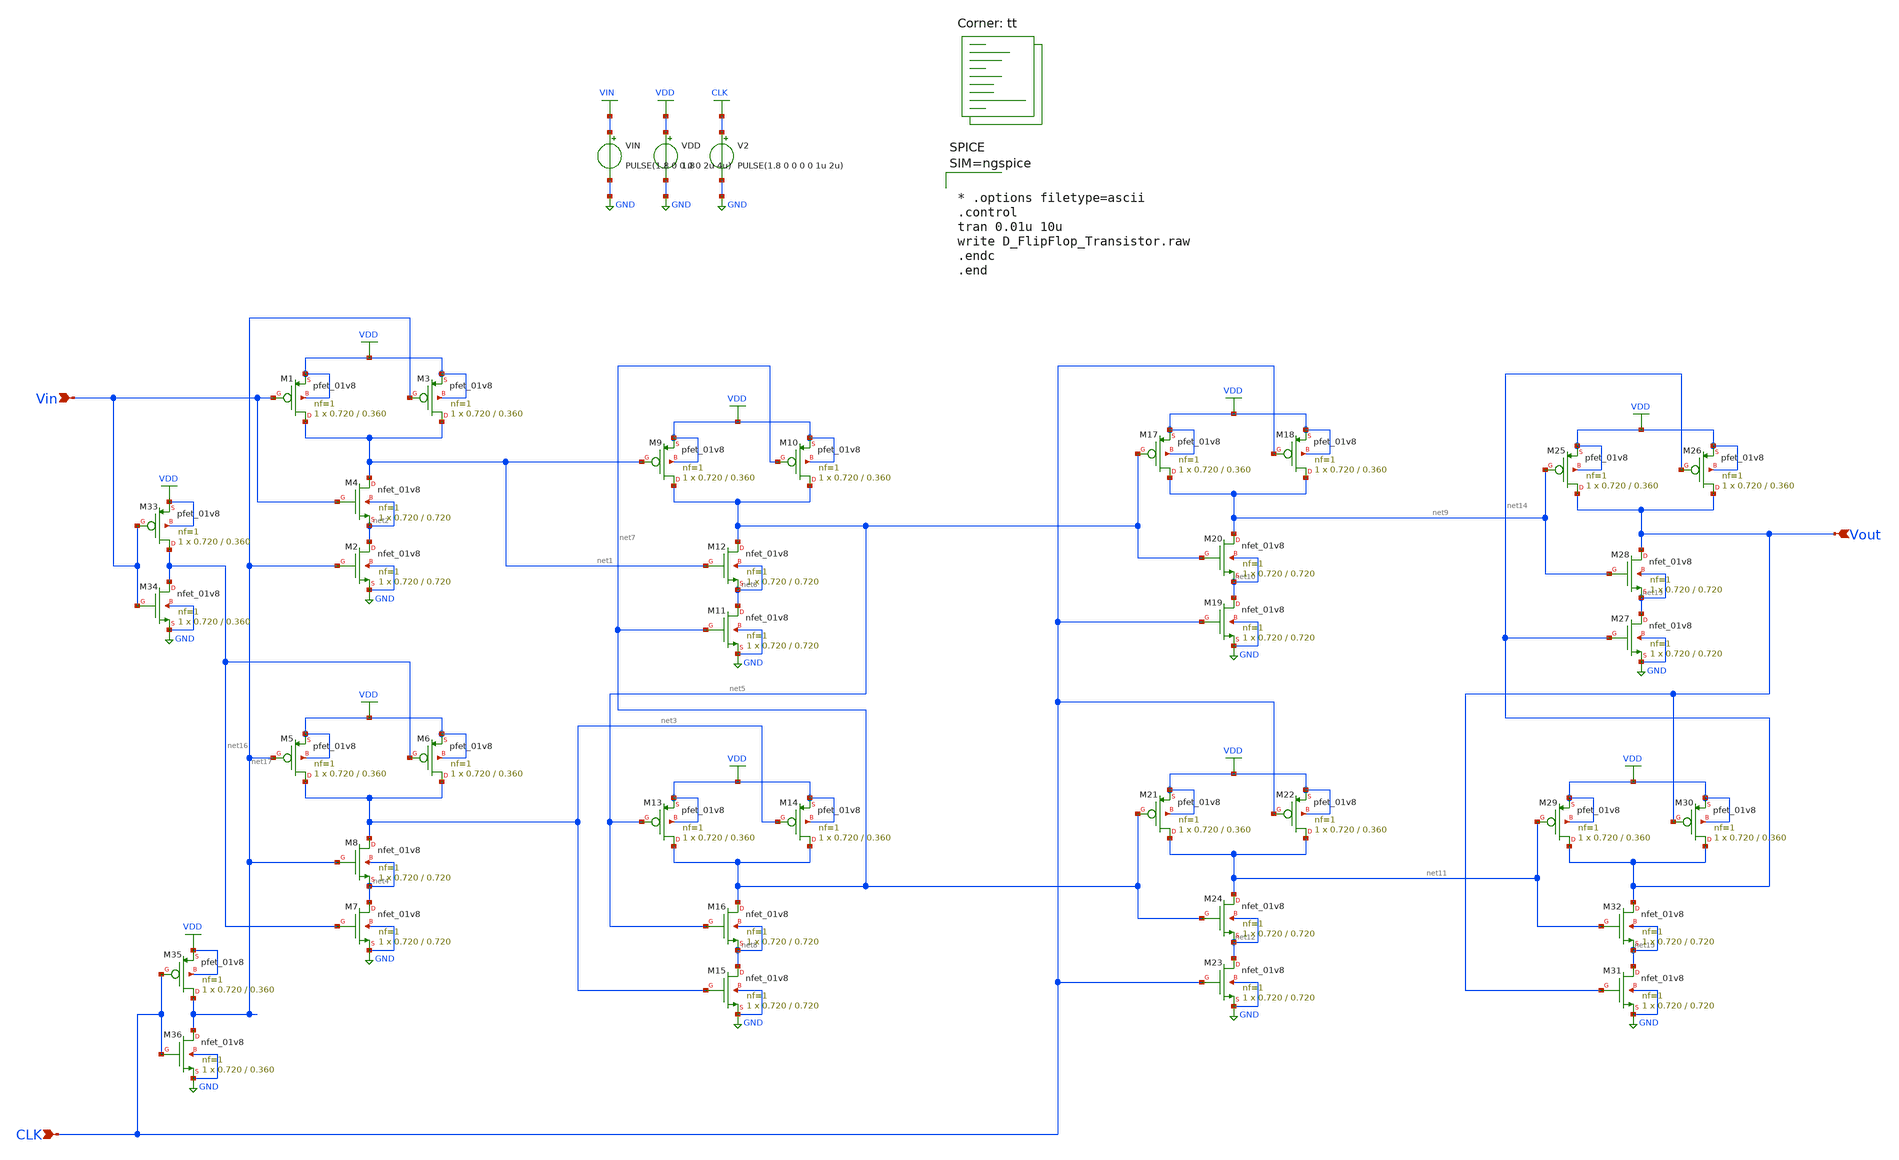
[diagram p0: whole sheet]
** sch_path: xschem/D_FlipFlop_Transistor.sch
**.subckt D_FlipFlop_Transistor CLK Vin Vout
*.ipin CLK
*.ipin Vin
*.ipin Vout
XM1 net1 Vin VDD VDD sky130_fd_pr__pfet_01v8 L=0.360 W=0.720 nf=1 ad='int((nf+1)/2) * W/nf * 0.29' as='int((nf+2)/2) * W/nf * 0.29'
+ pd='2*int((nf+1)/2) * (W/nf + 0.29)' ps='2*int((nf+2)/2) * (W/nf + 0.29)' nrd='0.29 / W' nrs='0.29 / W'
+ sa=0 sb=0 sd=0 mult=1 m=1
XM3 net1 net17 VDD VDD sky130_fd_pr__pfet_01v8 L=0.360 W=0.720 nf=1 ad='int((nf+1)/2) * W/nf * 0.29'
+ as='int((nf+2)/2) * W/nf * 0.29' pd='2*int((nf+1)/2) * (W/nf + 0.29)' ps='2*int((nf+2)/2) * (W/nf + 0.29)'
+ nrd='0.29 / W' nrs='0.29 / W' sa=0 sb=0 sd=0 mult=1 m=1
XM2 net2 net17 GND GND sky130_fd_pr__nfet_01v8 L=0.720 W=0.720 nf=1 ad='int((nf+1)/2) * W/nf * 0.29'
+ as='int((nf+2)/2) * W/nf * 0.29' pd='2*int((nf+1)/2) * (W/nf + 0.29)' ps='2*int((nf+2)/2) * (W/nf + 0.29)'
+ nrd='0.29 / W' nrs='0.29 / W' sa=0 sb=0 sd=0 mult=1 m=1
XM4 net1 Vin net2 net2 sky130_fd_pr__nfet_01v8 L=0.720 W=0.720 nf=1 ad='int((nf+1)/2) * W/nf * 0.29'
+ as='int((nf+2)/2) * W/nf * 0.29' pd='2*int((nf+1)/2) * (W/nf + 0.29)' ps='2*int((nf+2)/2) * (W/nf + 0.29)'
+ nrd='0.29 / W' nrs='0.29 / W' sa=0 sb=0 sd=0 mult=1 m=1
XM5 net3 net17 VDD VDD sky130_fd_pr__pfet_01v8 L=0.360 W=0.720 nf=1 ad='int((nf+1)/2) * W/nf * 0.29'
+ as='int((nf+2)/2) * W/nf * 0.29' pd='2*int((nf+1)/2) * (W/nf + 0.29)' ps='2*int((nf+2)/2) * (W/nf + 0.29)'
+ nrd='0.29 / W' nrs='0.29 / W' sa=0 sb=0 sd=0 mult=1 m=1
XM6 net3 net16 VDD VDD sky130_fd_pr__pfet_01v8 L=0.360 W=0.720 nf=1 ad='int((nf+1)/2) * W/nf * 0.29'
+ as='int((nf+2)/2) * W/nf * 0.29' pd='2*int((nf+1)/2) * (W/nf + 0.29)' ps='2*int((nf+2)/2) * (W/nf + 0.29)'
+ nrd='0.29 / W' nrs='0.29 / W' sa=0 sb=0 sd=0 mult=1 m=1
XM7 net4 net16 GND GND sky130_fd_pr__nfet_01v8 L=0.720 W=0.720 nf=1 ad='int((nf+1)/2) * W/nf * 0.29'
+ as='int((nf+2)/2) * W/nf * 0.29' pd='2*int((nf+1)/2) * (W/nf + 0.29)' ps='2*int((nf+2)/2) * (W/nf + 0.29)'
+ nrd='0.29 / W' nrs='0.29 / W' sa=0 sb=0 sd=0 mult=1 m=1
XM8 net3 net17 net4 net4 sky130_fd_pr__nfet_01v8 L=0.720 W=0.720 nf=1 ad='int((nf+1)/2) * W/nf * 0.29'
+ as='int((nf+2)/2) * W/nf * 0.29' pd='2*int((nf+1)/2) * (W/nf + 0.29)' ps='2*int((nf+2)/2) * (W/nf + 0.29)'
+ nrd='0.29 / W' nrs='0.29 / W' sa=0 sb=0 sd=0 mult=1 m=1
XM9 net5 net1 VDD VDD sky130_fd_pr__pfet_01v8 L=0.360 W=0.720 nf=1 ad='int((nf+1)/2) * W/nf * 0.29' as='int((nf+2)/2) * W/nf * 0.29'
+ pd='2*int((nf+1)/2) * (W/nf + 0.29)' ps='2*int((nf+2)/2) * (W/nf + 0.29)' nrd='0.29 / W' nrs='0.29 / W'
+ sa=0 sb=0 sd=0 mult=1 m=1
XM10 net5 net7 VDD VDD sky130_fd_pr__pfet_01v8 L=0.360 W=0.720 nf=1 ad='int((nf+1)/2) * W/nf * 0.29'
+ as='int((nf+2)/2) * W/nf * 0.29' pd='2*int((nf+1)/2) * (W/nf + 0.29)' ps='2*int((nf+2)/2) * (W/nf + 0.29)'
+ nrd='0.29 / W' nrs='0.29 / W' sa=0 sb=0 sd=0 mult=1 m=1
XM11 net6 net7 GND GND sky130_fd_pr__nfet_01v8 L=0.720 W=0.720 nf=1 ad='int((nf+1)/2) * W/nf * 0.29'
+ as='int((nf+2)/2) * W/nf * 0.29' pd='2*int((nf+1)/2) * (W/nf + 0.29)' ps='2*int((nf+2)/2) * (W/nf + 0.29)'
+ nrd='0.29 / W' nrs='0.29 / W' sa=0 sb=0 sd=0 mult=1 m=1
XM12 net5 net1 net6 net6 sky130_fd_pr__nfet_01v8 L=0.720 W=0.720 nf=1 ad='int((nf+1)/2) * W/nf * 0.29'
+ as='int((nf+2)/2) * W/nf * 0.29' pd='2*int((nf+1)/2) * (W/nf + 0.29)' ps='2*int((nf+2)/2) * (W/nf + 0.29)'
+ nrd='0.29 / W' nrs='0.29 / W' sa=0 sb=0 sd=0 mult=1 m=1
XM13 net7 net5 VDD VDD sky130_fd_pr__pfet_01v8 L=0.360 W=0.720 nf=1 ad='int((nf+1)/2) * W/nf * 0.29'
+ as='int((nf+2)/2) * W/nf * 0.29' pd='2*int((nf+1)/2) * (W/nf + 0.29)' ps='2*int((nf+2)/2) * (W/nf + 0.29)'
+ nrd='0.29 / W' nrs='0.29 / W' sa=0 sb=0 sd=0 mult=1 m=1
XM14 net7 net3 VDD VDD sky130_fd_pr__pfet_01v8 L=0.360 W=0.720 nf=1 ad='int((nf+1)/2) * W/nf * 0.29'
+ as='int((nf+2)/2) * W/nf * 0.29' pd='2*int((nf+1)/2) * (W/nf + 0.29)' ps='2*int((nf+2)/2) * (W/nf + 0.29)'
+ nrd='0.29 / W' nrs='0.29 / W' sa=0 sb=0 sd=0 mult=1 m=1
XM15 net8 net3 GND GND sky130_fd_pr__nfet_01v8 L=0.720 W=0.720 nf=1 ad='int((nf+1)/2) * W/nf * 0.29'
+ as='int((nf+2)/2) * W/nf * 0.29' pd='2*int((nf+1)/2) * (W/nf + 0.29)' ps='2*int((nf+2)/2) * (W/nf + 0.29)'
+ nrd='0.29 / W' nrs='0.29 / W' sa=0 sb=0 sd=0 mult=1 m=1
XM16 net7 net5 net8 net8 sky130_fd_pr__nfet_01v8 L=0.720 W=0.720 nf=1 ad='int((nf+1)/2) * W/nf * 0.29'
+ as='int((nf+2)/2) * W/nf * 0.29' pd='2*int((nf+1)/2) * (W/nf + 0.29)' ps='2*int((nf+2)/2) * (W/nf + 0.29)'
+ nrd='0.29 / W' nrs='0.29 / W' sa=0 sb=0 sd=0 mult=1 m=1
XM17 net9 net5 VDD VDD sky130_fd_pr__pfet_01v8 L=0.360 W=0.720 nf=1 ad='int((nf+1)/2) * W/nf * 0.29'
+ as='int((nf+2)/2) * W/nf * 0.29' pd='2*int((nf+1)/2) * (W/nf + 0.29)' ps='2*int((nf+2)/2) * (W/nf + 0.29)'
+ nrd='0.29 / W' nrs='0.29 / W' sa=0 sb=0 sd=0 mult=1 m=1
XM18 net9 CLK VDD VDD sky130_fd_pr__pfet_01v8 L=0.360 W=0.720 nf=1 ad='int((nf+1)/2) * W/nf * 0.29' as='int((nf+2)/2) * W/nf * 0.29'
+ pd='2*int((nf+1)/2) * (W/nf + 0.29)' ps='2*int((nf+2)/2) * (W/nf + 0.29)' nrd='0.29 / W' nrs='0.29 / W'
+ sa=0 sb=0 sd=0 mult=1 m=1
XM19 net10 CLK GND GND sky130_fd_pr__nfet_01v8 L=0.720 W=0.720 nf=1 ad='int((nf+1)/2) * W/nf * 0.29'
+ as='int((nf+2)/2) * W/nf * 0.29' pd='2*int((nf+1)/2) * (W/nf + 0.29)' ps='2*int((nf+2)/2) * (W/nf + 0.29)'
+ nrd='0.29 / W' nrs='0.29 / W' sa=0 sb=0 sd=0 mult=1 m=1
XM20 net9 net5 net10 net10 sky130_fd_pr__nfet_01v8 L=0.720 W=0.720 nf=1 ad='int((nf+1)/2) * W/nf * 0.29'
+ as='int((nf+2)/2) * W/nf * 0.29' pd='2*int((nf+1)/2) * (W/nf + 0.29)' ps='2*int((nf+2)/2) * (W/nf + 0.29)'
+ nrd='0.29 / W' nrs='0.29 / W' sa=0 sb=0 sd=0 mult=1 m=1
XM21 net11 net7 VDD VDD sky130_fd_pr__pfet_01v8 L=0.360 W=0.720 nf=1 ad='int((nf+1)/2) * W/nf * 0.29'
+ as='int((nf+2)/2) * W/nf * 0.29' pd='2*int((nf+1)/2) * (W/nf + 0.29)' ps='2*int((nf+2)/2) * (W/nf + 0.29)'
+ nrd='0.29 / W' nrs='0.29 / W' sa=0 sb=0 sd=0 mult=1 m=1
XM22 net11 CLK VDD VDD sky130_fd_pr__pfet_01v8 L=0.360 W=0.720 nf=1 ad='int((nf+1)/2) * W/nf * 0.29'
+ as='int((nf+2)/2) * W/nf * 0.29' pd='2*int((nf+1)/2) * (W/nf + 0.29)' ps='2*int((nf+2)/2) * (W/nf + 0.29)'
+ nrd='0.29 / W' nrs='0.29 / W' sa=0 sb=0 sd=0 mult=1 m=1
XM23 net12 CLK GND GND sky130_fd_pr__nfet_01v8 L=0.720 W=0.720 nf=1 ad='int((nf+1)/2) * W/nf * 0.29'
+ as='int((nf+2)/2) * W/nf * 0.29' pd='2*int((nf+1)/2) * (W/nf + 0.29)' ps='2*int((nf+2)/2) * (W/nf + 0.29)'
+ nrd='0.29 / W' nrs='0.29 / W' sa=0 sb=0 sd=0 mult=1 m=1
XM24 net11 net7 net12 net12 sky130_fd_pr__nfet_01v8 L=0.720 W=0.720 nf=1 ad='int((nf+1)/2) * W/nf * 0.29'
+ as='int((nf+2)/2) * W/nf * 0.29' pd='2*int((nf+1)/2) * (W/nf + 0.29)' ps='2*int((nf+2)/2) * (W/nf + 0.29)'
+ nrd='0.29 / W' nrs='0.29 / W' sa=0 sb=0 sd=0 mult=1 m=1
XM25 Vout net9 VDD VDD sky130_fd_pr__pfet_01v8 L=0.360 W=0.720 nf=1 ad='int((nf+1)/2) * W/nf * 0.29'
+ as='int((nf+2)/2) * W/nf * 0.29' pd='2*int((nf+1)/2) * (W/nf + 0.29)' ps='2*int((nf+2)/2) * (W/nf + 0.29)'
+ nrd='0.29 / W' nrs='0.29 / W' sa=0 sb=0 sd=0 mult=1 m=1
XM26 Vout net14 VDD VDD sky130_fd_pr__pfet_01v8 L=0.360 W=0.720 nf=1 ad='int((nf+1)/2) * W/nf * 0.29'
+ as='int((nf+2)/2) * W/nf * 0.29' pd='2*int((nf+1)/2) * (W/nf + 0.29)' ps='2*int((nf+2)/2) * (W/nf + 0.29)'
+ nrd='0.29 / W' nrs='0.29 / W' sa=0 sb=0 sd=0 mult=1 m=1
XM27 net13 net14 GND GND sky130_fd_pr__nfet_01v8 L=0.720 W=0.720 nf=1 ad='int((nf+1)/2) * W/nf * 0.29'
+ as='int((nf+2)/2) * W/nf * 0.29' pd='2*int((nf+1)/2) * (W/nf + 0.29)' ps='2*int((nf+2)/2) * (W/nf + 0.29)'
+ nrd='0.29 / W' nrs='0.29 / W' sa=0 sb=0 sd=0 mult=1 m=1
XM28 Vout net9 net13 net13 sky130_fd_pr__nfet_01v8 L=0.720 W=0.720 nf=1 ad='int((nf+1)/2) * W/nf * 0.29'
+ as='int((nf+2)/2) * W/nf * 0.29' pd='2*int((nf+1)/2) * (W/nf + 0.29)' ps='2*int((nf+2)/2) * (W/nf + 0.29)'
+ nrd='0.29 / W' nrs='0.29 / W' sa=0 sb=0 sd=0 mult=1 m=1
XM29 net14 net11 VDD VDD sky130_fd_pr__pfet_01v8 L=0.360 W=0.720 nf=1 ad='int((nf+1)/2) * W/nf * 0.29'
+ as='int((nf+2)/2) * W/nf * 0.29' pd='2*int((nf+1)/2) * (W/nf + 0.29)' ps='2*int((nf+2)/2) * (W/nf + 0.29)'
+ nrd='0.29 / W' nrs='0.29 / W' sa=0 sb=0 sd=0 mult=1 m=1
XM30 net14 Vout VDD VDD sky130_fd_pr__pfet_01v8 L=0.360 W=0.720 nf=1 ad='int((nf+1)/2) * W/nf * 0.29'
+ as='int((nf+2)/2) * W/nf * 0.29' pd='2*int((nf+1)/2) * (W/nf + 0.29)' ps='2*int((nf+2)/2) * (W/nf + 0.29)'
+ nrd='0.29 / W' nrs='0.29 / W' sa=0 sb=0 sd=0 mult=1 m=1
XM31 net15 Vout GND GND sky130_fd_pr__nfet_01v8 L=0.720 W=0.720 nf=1 ad='int((nf+1)/2) * W/nf * 0.29'
+ as='int((nf+2)/2) * W/nf * 0.29' pd='2*int((nf+1)/2) * (W/nf + 0.29)' ps='2*int((nf+2)/2) * (W/nf + 0.29)'
+ nrd='0.29 / W' nrs='0.29 / W' sa=0 sb=0 sd=0 mult=1 m=1
XM32 net14 net11 net15 net15 sky130_fd_pr__nfet_01v8 L=0.720 W=0.720 nf=1 ad='int((nf+1)/2) * W/nf * 0.29'
+ as='int((nf+2)/2) * W/nf * 0.29' pd='2*int((nf+1)/2) * (W/nf + 0.29)' ps='2*int((nf+2)/2) * (W/nf + 0.29)'
+ nrd='0.29 / W' nrs='0.29 / W' sa=0 sb=0 sd=0 mult=1 m=1
XM33 net16 Vin VDD VDD sky130_fd_pr__pfet_01v8 L=0.360 W=0.720 nf=1 ad='int((nf+1)/2) * W/nf * 0.29'
+ as='int((nf+2)/2) * W/nf * 0.29' pd='2*int((nf+1)/2) * (W/nf + 0.29)' ps='2*int((nf+2)/2) * (W/nf + 0.29)'
+ nrd='0.29 / W' nrs='0.29 / W' sa=0 sb=0 sd=0 mult=1 m=1
XM34 net16 Vin GND GND sky130_fd_pr__nfet_01v8 L=0.360 W=0.720 nf=1 ad='int((nf+1)/2) * W/nf * 0.29'
+ as='int((nf+2)/2) * W/nf * 0.29' pd='2*int((nf+1)/2) * (W/nf + 0.29)' ps='2*int((nf+2)/2) * (W/nf + 0.29)'
+ nrd='0.29 / W' nrs='0.29 / W' sa=0 sb=0 sd=0 mult=1 m=1
XM35 net17 CLK VDD VDD sky130_fd_pr__pfet_01v8 L=0.360 W=0.720 nf=1 ad='int((nf+1)/2) * W/nf * 0.29'
+ as='int((nf+2)/2) * W/nf * 0.29' pd='2*int((nf+1)/2) * (W/nf + 0.29)' ps='2*int((nf+2)/2) * (W/nf + 0.29)'
+ nrd='0.29 / W' nrs='0.29 / W' sa=0 sb=0 sd=0 mult=1 m=1
XM36 net17 CLK GND GND sky130_fd_pr__nfet_01v8 L=0.360 W=0.720 nf=1 ad='int((nf+1)/2) * W/nf * 0.29'
+ as='int((nf+2)/2) * W/nf * 0.29' pd='2*int((nf+1)/2) * (W/nf + 0.29)' ps='2*int((nf+2)/2) * (W/nf + 0.29)'
+ nrd='0.29 / W' nrs='0.29 / W' sa=0 sb=0 sd=0 mult=1 m=1
VDD VDD GND 1.8
V2 CLK GND PULSE(1.8 0 0 0 0 1u 2u)
VIN VIN GND PULSE(1.8 0 0 0 0 2u 4u)
**** begin user architecture code
.lib $::SKYWATER_MODELS/sky130.lib.spice tt



* .options filetype=ascii
.control
tran 0.01u 10u
write D_FlipFlop_Transistor.raw
.endc
.end



**** end user architecture code
**.ends
.GLOBAL VDD
.GLOBAL GND
.GLOBAL CLK
.GLOBAL VIN
.end
